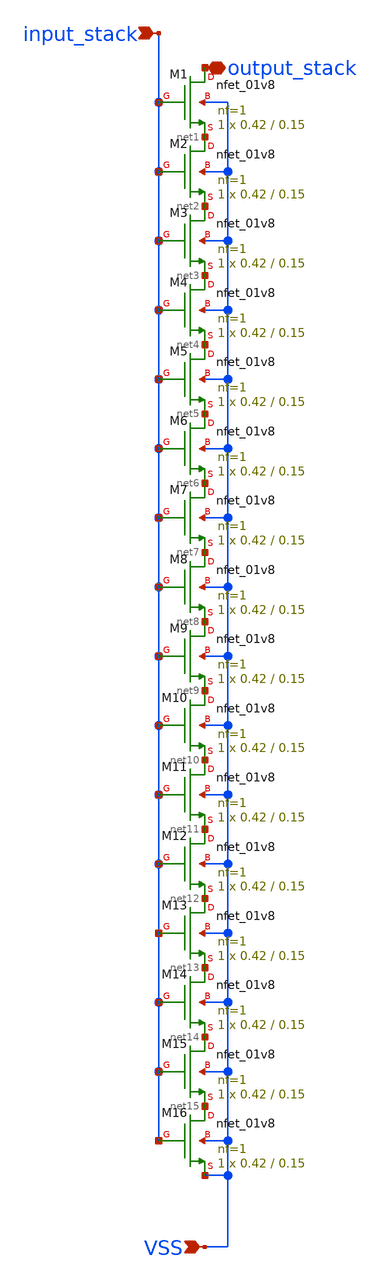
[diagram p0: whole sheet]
** sch_path: hgu/xschem/hgu_nfet_hvt_stack_in_delay.sch
**.subckt hgu_nfet_hvt_stack_in_delay VSS input_stack output_stack
*.ipin VSS
*.ipin input_stack
*.iopin output_stack
XM1 output_stack input_stack net1 VSS sky130_fd_pr__nfet_01v8 L=0.15 W=0.42 nf=1 ad='int((nf+1)/2) * W/nf * 0.29'
+ as='int((nf+2)/2) * W/nf * 0.29' pd='2*int((nf+1)/2) * (W/nf + 0.29)' ps='2*int((nf+2)/2) * (W/nf + 0.29)'
+ nrd='0.29 / W' nrs='0.29 / W' sa=0 sb=0 sd=0 mult=1 m=1
XM2 net1 input_stack net2 VSS sky130_fd_pr__nfet_01v8 L=0.15 W=0.42 nf=1 ad='int((nf+1)/2) * W/nf * 0.29'
+ as='int((nf+2)/2) * W/nf * 0.29' pd='2*int((nf+1)/2) * (W/nf + 0.29)' ps='2*int((nf+2)/2) * (W/nf + 0.29)'
+ nrd='0.29 / W' nrs='0.29 / W' sa=0 sb=0 sd=0 mult=1 m=1
XM3 net2 input_stack net3 VSS sky130_fd_pr__nfet_01v8 L=0.15 W=0.42 nf=1 ad='int((nf+1)/2) * W/nf * 0.29'
+ as='int((nf+2)/2) * W/nf * 0.29' pd='2*int((nf+1)/2) * (W/nf + 0.29)' ps='2*int((nf+2)/2) * (W/nf + 0.29)'
+ nrd='0.29 / W' nrs='0.29 / W' sa=0 sb=0 sd=0 mult=1 m=1
XM4 net3 input_stack net4 VSS sky130_fd_pr__nfet_01v8 L=0.15 W=0.42 nf=1 ad='int((nf+1)/2) * W/nf * 0.29'
+ as='int((nf+2)/2) * W/nf * 0.29' pd='2*int((nf+1)/2) * (W/nf + 0.29)' ps='2*int((nf+2)/2) * (W/nf + 0.29)'
+ nrd='0.29 / W' nrs='0.29 / W' sa=0 sb=0 sd=0 mult=1 m=1
XM5 net4 input_stack net5 VSS sky130_fd_pr__nfet_01v8 L=0.15 W=0.42 nf=1 ad='int((nf+1)/2) * W/nf * 0.29'
+ as='int((nf+2)/2) * W/nf * 0.29' pd='2*int((nf+1)/2) * (W/nf + 0.29)' ps='2*int((nf+2)/2) * (W/nf + 0.29)'
+ nrd='0.29 / W' nrs='0.29 / W' sa=0 sb=0 sd=0 mult=1 m=1
XM6 net5 input_stack net6 VSS sky130_fd_pr__nfet_01v8 L=0.15 W=0.42 nf=1 ad='int((nf+1)/2) * W/nf * 0.29'
+ as='int((nf+2)/2) * W/nf * 0.29' pd='2*int((nf+1)/2) * (W/nf + 0.29)' ps='2*int((nf+2)/2) * (W/nf + 0.29)'
+ nrd='0.29 / W' nrs='0.29 / W' sa=0 sb=0 sd=0 mult=1 m=1
XM7 net6 input_stack net7 VSS sky130_fd_pr__nfet_01v8 L=0.15 W=0.42 nf=1 ad='int((nf+1)/2) * W/nf * 0.29'
+ as='int((nf+2)/2) * W/nf * 0.29' pd='2*int((nf+1)/2) * (W/nf + 0.29)' ps='2*int((nf+2)/2) * (W/nf + 0.29)'
+ nrd='0.29 / W' nrs='0.29 / W' sa=0 sb=0 sd=0 mult=1 m=1
XM8 net7 input_stack net8 VSS sky130_fd_pr__nfet_01v8 L=0.15 W=0.42 nf=1 ad='int((nf+1)/2) * W/nf * 0.29'
+ as='int((nf+2)/2) * W/nf * 0.29' pd='2*int((nf+1)/2) * (W/nf + 0.29)' ps='2*int((nf+2)/2) * (W/nf + 0.29)'
+ nrd='0.29 / W' nrs='0.29 / W' sa=0 sb=0 sd=0 mult=1 m=1
XM9 net8 input_stack net9 VSS sky130_fd_pr__nfet_01v8 L=0.15 W=0.42 nf=1 ad='int((nf+1)/2) * W/nf * 0.29'
+ as='int((nf+2)/2) * W/nf * 0.29' pd='2*int((nf+1)/2) * (W/nf + 0.29)' ps='2*int((nf+2)/2) * (W/nf + 0.29)'
+ nrd='0.29 / W' nrs='0.29 / W' sa=0 sb=0 sd=0 mult=1 m=1
XM10 net9 input_stack net10 VSS sky130_fd_pr__nfet_01v8 L=0.15 W=0.42 nf=1 ad='int((nf+1)/2) * W/nf * 0.29'
+ as='int((nf+2)/2) * W/nf * 0.29' pd='2*int((nf+1)/2) * (W/nf + 0.29)' ps='2*int((nf+2)/2) * (W/nf + 0.29)'
+ nrd='0.29 / W' nrs='0.29 / W' sa=0 sb=0 sd=0 mult=1 m=1
XM11 net10 input_stack net11 VSS sky130_fd_pr__nfet_01v8 L=0.15 W=0.42 nf=1 ad='int((nf+1)/2) * W/nf * 0.29'
+ as='int((nf+2)/2) * W/nf * 0.29' pd='2*int((nf+1)/2) * (W/nf + 0.29)' ps='2*int((nf+2)/2) * (W/nf + 0.29)'
+ nrd='0.29 / W' nrs='0.29 / W' sa=0 sb=0 sd=0 mult=1 m=1
XM12 net11 input_stack net12 VSS sky130_fd_pr__nfet_01v8 L=0.15 W=0.42 nf=1 ad='int((nf+1)/2) * W/nf * 0.29'
+ as='int((nf+2)/2) * W/nf * 0.29' pd='2*int((nf+1)/2) * (W/nf + 0.29)' ps='2*int((nf+2)/2) * (W/nf + 0.29)'
+ nrd='0.29 / W' nrs='0.29 / W' sa=0 sb=0 sd=0 mult=1 m=1
XM13 net12 input_stack net13 VSS sky130_fd_pr__nfet_01v8 L=0.15 W=0.42 nf=1 ad='int((nf+1)/2) * W/nf * 0.29'
+ as='int((nf+2)/2) * W/nf * 0.29' pd='2*int((nf+1)/2) * (W/nf + 0.29)' ps='2*int((nf+2)/2) * (W/nf + 0.29)'
+ nrd='0.29 / W' nrs='0.29 / W' sa=0 sb=0 sd=0 mult=1 m=1
XM14 net13 input_stack net14 VSS sky130_fd_pr__nfet_01v8 L=0.15 W=0.42 nf=1 ad='int((nf+1)/2) * W/nf * 0.29'
+ as='int((nf+2)/2) * W/nf * 0.29' pd='2*int((nf+1)/2) * (W/nf + 0.29)' ps='2*int((nf+2)/2) * (W/nf + 0.29)'
+ nrd='0.29 / W' nrs='0.29 / W' sa=0 sb=0 sd=0 mult=1 m=1
XM15 net14 input_stack net15 VSS sky130_fd_pr__nfet_01v8 L=0.15 W=0.42 nf=1 ad='int((nf+1)/2) * W/nf * 0.29'
+ as='int((nf+2)/2) * W/nf * 0.29' pd='2*int((nf+1)/2) * (W/nf + 0.29)' ps='2*int((nf+2)/2) * (W/nf + 0.29)'
+ nrd='0.29 / W' nrs='0.29 / W' sa=0 sb=0 sd=0 mult=1 m=1
XM16 net15 input_stack VSS VSS sky130_fd_pr__nfet_01v8 L=0.15 W=0.42 nf=1 ad='int((nf+1)/2) * W/nf * 0.29'
+ as='int((nf+2)/2) * W/nf * 0.29' pd='2*int((nf+1)/2) * (W/nf + 0.29)' ps='2*int((nf+2)/2) * (W/nf + 0.29)'
+ nrd='0.29 / W' nrs='0.29 / W' sa=0 sb=0 sd=0 mult=1 m=1
**.ends
.end
